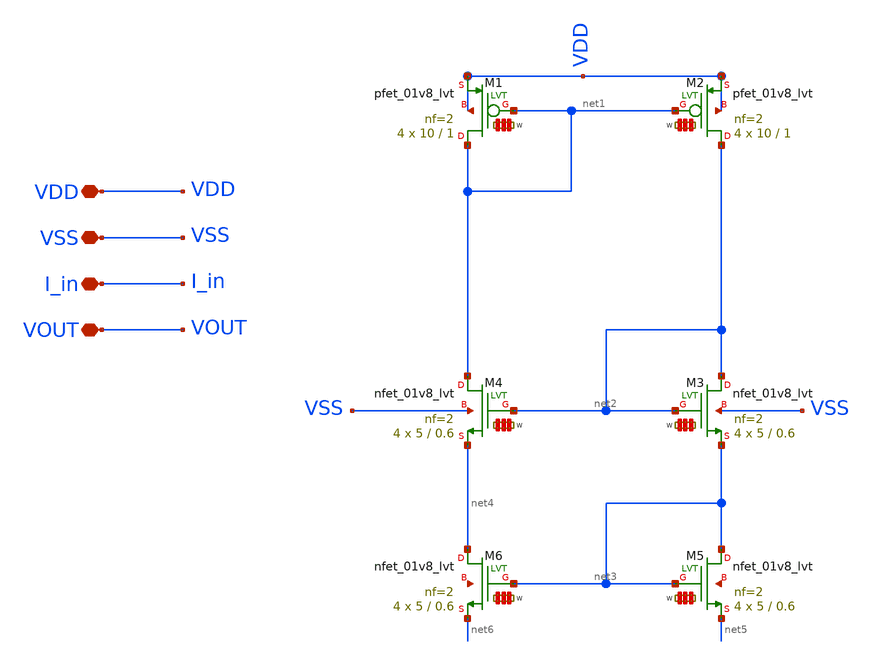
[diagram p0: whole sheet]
** sch_path: my_ip/sky130A/TIA_1_8_V2/TI.sch
**.subckt TI VDD VSS I_in VOUT
*.iopin VDD
*.iopin VSS
*.iopin I_in
*.iopin VOUT
XM1 net1 net1 VDD VDD sky130_fd_pr__pfet_01v8_lvt L=1 W='10 * 2 ' nf=2 ad='int((2 + 1)/2) * 10 / 2 * 0.29'
+ as='int((2 + 2)/2) * 10 / 2 * 0.29' pd='2*int((2 + 1)/2) * (10 / 2 + 0.29)' ps='2*int((2 + 2)/2) * (10 / 2 + 0.29)'
+ nrd='0.29 / 10 ' nrs='0.29 / 10 ' sa=0 sb=0 sd=0 mult=4 m=4
XM2 net2 net1 VDD VDD sky130_fd_pr__pfet_01v8_lvt L=1 W='10 * 2 ' nf=2 ad='int((2 + 1)/2) * 10 / 2 * 0.29'
+ as='int((2 + 2)/2) * 10 / 2 * 0.29' pd='2*int((2 + 1)/2) * (10 / 2 + 0.29)' ps='2*int((2 + 2)/2) * (10 / 2 + 0.29)'
+ nrd='0.29 / 10 ' nrs='0.29 / 10 ' sa=0 sb=0 sd=0 mult=4 m=4
XM3 net2 net2 net3 VSS sky130_fd_pr__nfet_01v8_lvt L=0.6 W='5 * 2 ' nf=2 ad='int((2 + 1)/2) * 5 / 2 * 0.29'
+ as='int((2 + 2)/2) * 5 / 2 * 0.29' pd='2*int((2 + 1)/2) * (5 / 2 + 0.29)' ps='2*int((2 + 2)/2) * (5 / 2 + 0.29)'
+ nrd='0.29 / 5 ' nrs='0.29 / 5 ' sa=0 sb=0 sd=0 mult=4 m=4
XM4 net1 net2 net4 VSS sky130_fd_pr__nfet_01v8_lvt L=0.6 W='5 * 2 ' nf=2 ad='int((2 + 1)/2) * 5 / 2 * 0.29'
+ as='int((2 + 2)/2) * 5 / 2 * 0.29' pd='2*int((2 + 1)/2) * (5 / 2 + 0.29)' ps='2*int((2 + 2)/2) * (5 / 2 + 0.29)'
+ nrd='0.29 / 5 ' nrs='0.29 / 5 ' sa=0 sb=0 sd=0 mult=4 m=4
XM5 net3 net3 net5 net7 sky130_fd_pr__nfet_01v8_lvt L=0.6 W='5 * 2 ' nf=2 ad='int((2 + 1)/2) * 5 / 2 * 0.29'
+ as='int((2 + 2)/2) * 5 / 2 * 0.29' pd='2*int((2 + 1)/2) * (5 / 2 + 0.29)' ps='2*int((2 + 2)/2) * (5 / 2 + 0.29)'
+ nrd='0.29 / 5 ' nrs='0.29 / 5 ' sa=0 sb=0 sd=0 mult=4 m=4
XM6 net4 net3 net6 net8 sky130_fd_pr__nfet_01v8_lvt L=0.6 W='5 * 2 ' nf=2 ad='int((2 + 1)/2) * 5 / 2 * 0.29'
+ as='int((2 + 2)/2) * 5 / 2 * 0.29' pd='2*int((2 + 1)/2) * (5 / 2 + 0.29)' ps='2*int((2 + 2)/2) * (5 / 2 + 0.29)'
+ nrd='0.29 / 5 ' nrs='0.29 / 5 ' sa=0 sb=0 sd=0 mult=4 m=4
**.ends
.end
